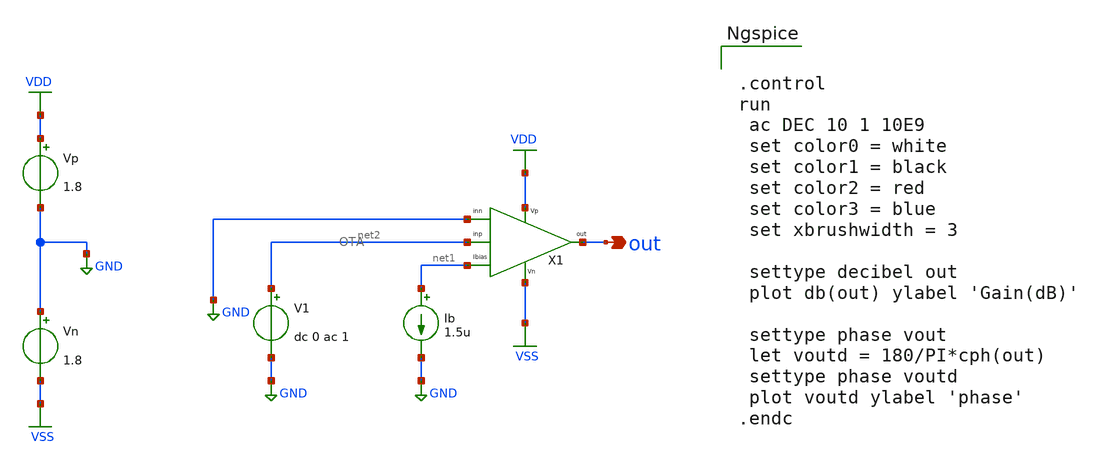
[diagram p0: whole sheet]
** sch_path: xschem/Tb_OTA.sch
**.subckt Tb_OTA out
*.opin out
V1 net2 GND dc 0 ac 1
Ib net1 GND 1.5u
X1 VDD VSS net1 out net2 GND OTA
Vn GND VSS 1.8
Vp VDD GND 1.8
**** begin user architecture code

.lib /edatools/pdks/skywater-pdk/libraries/sky130_fd_pr_ngspice/latest/models/sky130.lib.spice tt



.control
run
 ac DEC 10 1 10E9
 set color0 = white
 set color1 = black
 set color2 = red
 set color3 = blue
 set xbrushwidth = 3

 settype decibel out
 plot db(out) ylabel 'Gain(dB)'

 settype phase vout
 let voutd = 180/PI*cph(out)
 settype phase voutd
 plot voutd ylabel 'phase'
.endc


**** end user architecture code
**.ends

* expanding   symbol:  OTA.sym # of pins=6
** sym_path: xschem/OTA.sym
** sch_path: xschem/OTA.sch
.subckt OTA Vp Vn ib vout inp inn
*.ipin inp
*.ipin inn
*.opin vout
*.iopin Vp
*.iopin Vn
*.ipin ib
XM7 net1 net1 Vp Vp sky130_fd_pr__pfet_01v8 L=1 W=1.4 nf=1 ad='int((nf+1)/2) * W/nf * 0.29' as='int((nf+2)/2) * W/nf * 0.29'
+ pd='2*int((nf+1)/2) * (W/nf + 0.29)' ps='2*int((nf+2)/2) * (W/nf + 0.29)' nrd='0.29 / W' nrs='0.29 / W'
+ sa=0 sb=0 sd=0 mult=1 m=1
XM8 vout net1 Vp Vp sky130_fd_pr__pfet_01v8 L=1 W=1.4 nf=1 ad='int((nf+1)/2) * W/nf * 0.29' as='int((nf+2)/2) * W/nf * 0.29'
+ pd='2*int((nf+1)/2) * (W/nf + 0.29)' ps='2*int((nf+2)/2) * (W/nf + 0.29)' nrd='0.29 / W' nrs='0.29 / W'
+ sa=0 sb=0 sd=0 mult=1 m=1
XM9 ib ib Vp Vp sky130_fd_pr__pfet_01v8 L=4 W=5 nf=1 ad='int((nf+1)/2) * W/nf * 0.29' as='int((nf+2)/2) * W/nf * 0.29'
+ pd='2*int((nf+1)/2) * (W/nf + 0.29)' ps='2*int((nf+2)/2) * (W/nf + 0.29)' nrd='0.29 / W' nrs='0.29 / W'
+ sa=0 sb=0 sd=0 mult=1 m=1
XM10 net4 ib Vp Vp sky130_fd_pr__pfet_01v8 L=4 W=5 nf=1 ad='int((nf+1)/2) * W/nf * 0.29' as='int((nf+2)/2) * W/nf * 0.29'
+ pd='2*int((nf+1)/2) * (W/nf + 0.29)' ps='2*int((nf+2)/2) * (W/nf + 0.29)' nrd='0.29 / W' nrs='0.29 / W'
+ sa=0 sb=0 sd=0 mult=1 m=1
XM1 net2 inp net4 Vp sky130_fd_pr__pfet_01v8 L=2 W=1.7 nf=1 ad='int((nf+1)/2) * W/nf * 0.29' as='int((nf+2)/2) * W/nf * 0.29'
+ pd='2*int((nf+1)/2) * (W/nf + 0.29)' ps='2*int((nf+2)/2) * (W/nf + 0.29)' nrd='0.29 / W' nrs='0.29 / W'
+ sa=0 sb=0 sd=0 mult=1 m=1
XM2 net3 inn net4 Vp sky130_fd_pr__pfet_01v8 L=2 W=1.7 nf=1 ad='int((nf+1)/2) * W/nf * 0.29' as='int((nf+2)/2) * W/nf * 0.29'
+ pd='2*int((nf+1)/2) * (W/nf + 0.29)' ps='2*int((nf+2)/2) * (W/nf + 0.29)' nrd='0.29 / W' nrs='0.29 / W'
+ sa=0 sb=0 sd=0 mult=1 m=1
XM3 net2 net2 Vn Vn sky130_fd_pr__nfet_01v8 L=4 W=0.8 nf=1 ad='int((nf+1)/2) * W/nf * 0.29' as='int((nf+2)/2) * W/nf * 0.29'
+ pd='2*int((nf+1)/2) * (W/nf + 0.29)' ps='2*int((nf+2)/2) * (W/nf + 0.29)' nrd='0.29 / W' nrs='0.29 / W'
+ sa=0 sb=0 sd=0 mult=1 m=1
XM4 net3 net3 Vn Vn sky130_fd_pr__nfet_01v8 L=4 W=0.8 nf=1 ad='int((nf+1)/2) * W/nf * 0.29' as='int((nf+2)/2) * W/nf * 0.29'
+ pd='2*int((nf+1)/2) * (W/nf + 0.29)' ps='2*int((nf+2)/2) * (W/nf + 0.29)' nrd='0.29 / W' nrs='0.29 / W'
+ sa=0 sb=0 sd=0 mult=1 m=1
XM6 vout net3 Vn Vn sky130_fd_pr__nfet_01v8 L=4 W=0.8 nf=1 ad='int((nf+1)/2) * W/nf * 0.29' as='int((nf+2)/2) * W/nf * 0.29'
+ pd='2*int((nf+1)/2) * (W/nf + 0.29)' ps='2*int((nf+2)/2) * (W/nf + 0.29)' nrd='0.29 / W' nrs='0.29 / W'
+ sa=0 sb=0 sd=0 mult=1 m=1
XM5 net1 net2 Vn Vn sky130_fd_pr__nfet_01v8 L=4 W=0.8 nf=1 ad='int((nf+1)/2) * W/nf * 0.29' as='int((nf+2)/2) * W/nf * 0.29'
+ pd='2*int((nf+1)/2) * (W/nf + 0.29)' ps='2*int((nf+2)/2) * (W/nf + 0.29)' nrd='0.29 / W' nrs='0.29 / W'
+ sa=0 sb=0 sd=0 mult=1 m=1
.ends

.GLOBAL VDD
.GLOBAL GND
.GLOBAL VSS
.end
